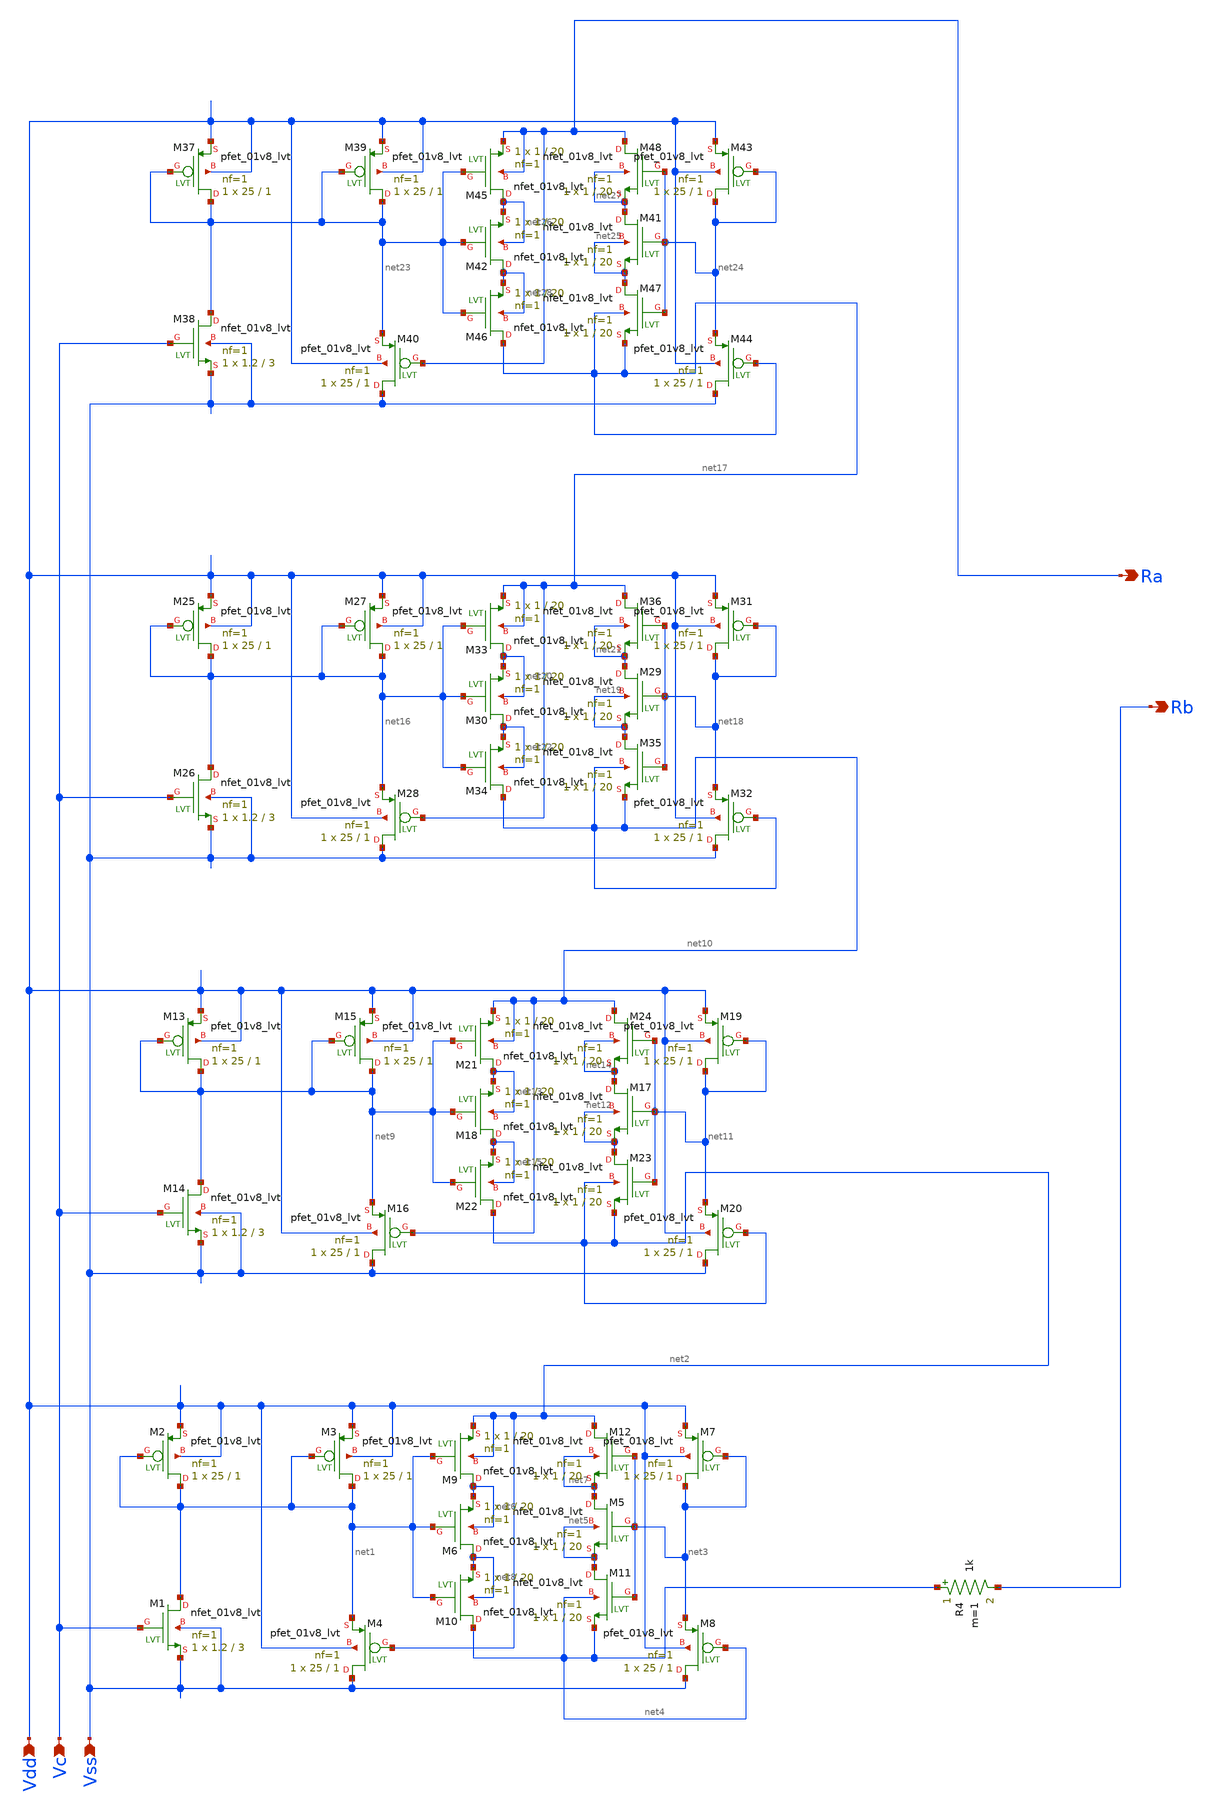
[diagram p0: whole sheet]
** sch_path: xschem/Active_Res.sch
**.subckt Active_Res Vss Vdd Vc Ra Rb
*.ipin Vss
*.ipin Vdd
*.ipin Vc
*.opin Ra
*.opin Rb
XM2 net1 net1 Vdd Vdd sky130_fd_pr__pfet_01v8_lvt L=1 W=25 nf=1 ad='int((1 + 1)/2) * 25 / 1 * 0.29' as='int((1 + 2)/2) * 25 / 1 * 0.29'
+ pd='2*int((1 + 1)/2) * (25 / 1 + 0.29)' ps='2*int((1 + 2)/2) * (25 / 1 + 0.29)' nrd='0.29 / 25 ' nrs='0.29 / 25 '
+ sa=0 sb=0 sd=0 mult=1 m=1
XM1 net1 Vc Vss Vss sky130_fd_pr__nfet_01v8_lvt L=3 W=1.2 nf=1 ad='int((1 + 1)/2) * 1.2 / 1 * 0.29' as='int((1 + 2)/2) * 1.2 / 1 * 0.29'
+ pd='2*int((1 + 1)/2) * (1.2 / 1 + 0.29)' ps='2*int((1 + 2)/2) * (1.2 / 1 + 0.29)' nrd='0.29 / 1.2 ' nrs='0.29 / 1.2 '
+ sa=0 sb=0 sd=0 mult=1 m=1
XM3 net1 net1 Vdd Vdd sky130_fd_pr__pfet_01v8_lvt L=1 W=25 nf=1 ad='int((1 + 1)/2) * 25 / 1 * 0.29' as='int((1 + 2)/2) * 25 / 1 * 0.29'
+ pd='2*int((1 + 1)/2) * (25 / 1 + 0.29)' ps='2*int((1 + 2)/2) * (25 / 1 + 0.29)' nrd='0.29 / 25 ' nrs='0.29 / 25 '
+ sa=0 sb=0 sd=0 mult=1 m=1
XM4 Vss net2 net1 Vdd sky130_fd_pr__pfet_01v8_lvt L=1 W=25 nf=1 ad='int((1 + 1)/2) * 25 / 1 * 0.29' as='int((1 + 2)/2) * 25 / 1 * 0.29'
+ pd='2*int((1 + 1)/2) * (25 / 1 + 0.29)' ps='2*int((1 + 2)/2) * (25 / 1 + 0.29)' nrd='0.29 / 25 ' nrs='0.29 / 25 '
+ sa=0 sb=0 sd=0 mult=1 m=1
XM5 net7 net3 net5 net5 sky130_fd_pr__nfet_01v8_lvt L=20 W=1 nf=1 ad='int((1 + 1)/2) * 1 / 1 * 0.29'
+ as='int((1 + 2)/2) * 1 / 1 * 0.29' pd='2*int((1 + 1)/2) * (1 / 1 + 0.29)' ps='2*int((1 + 2)/2) * (1 / 1 + 0.29)'
+ nrd='0.29 / 1 ' nrs='0.29 / 1 ' sa=0 sb=0 sd=0 mult=1 m=1
XM6 net8 net1 net6 net6 sky130_fd_pr__nfet_01v8_lvt L=20 W=1 nf=1 ad='int((1 + 1)/2) * 1 / 1 * 0.29'
+ as='int((1 + 2)/2) * 1 / 1 * 0.29' pd='2*int((1 + 1)/2) * (1 / 1 + 0.29)' ps='2*int((1 + 2)/2) * (1 / 1 + 0.29)'
+ nrd='0.29 / 1 ' nrs='0.29 / 1 ' sa=0 sb=0 sd=0 mult=1 m=1
XM7 net3 net3 Vdd Vdd sky130_fd_pr__pfet_01v8_lvt L=1 W=25 nf=1 ad='int((1 + 1)/2) * 25 / 1 * 0.29' as='int((1 + 2)/2) * 25 / 1 * 0.29'
+ pd='2*int((1 + 1)/2) * (25 / 1 + 0.29)' ps='2*int((1 + 2)/2) * (25 / 1 + 0.29)' nrd='0.29 / 25 ' nrs='0.29 / 25 '
+ sa=0 sb=0 sd=0 mult=1 m=1
XM8 Vss net4 net3 Vdd sky130_fd_pr__pfet_01v8_lvt L=1 W=25 nf=1 ad='int((1 + 1)/2) * 25 / 1 * 0.29' as='int((1 + 2)/2) * 25 / 1 * 0.29'
+ pd='2*int((1 + 1)/2) * (25 / 1 + 0.29)' ps='2*int((1 + 2)/2) * (25 / 1 + 0.29)' nrd='0.29 / 25 ' nrs='0.29 / 25 '
+ sa=0 sb=0 sd=0 mult=1 m=1
R4 net4 Rb 1k m=1
XM9 net6 net1 net2 net2 sky130_fd_pr__nfet_01v8_lvt L=20 W=1 nf=1 ad='int((1 + 1)/2) * 1 / 1 * 0.29'
+ as='int((1 + 2)/2) * 1 / 1 * 0.29' pd='2*int((1 + 1)/2) * (1 / 1 + 0.29)' ps='2*int((1 + 2)/2) * (1 / 1 + 0.29)'
+ nrd='0.29 / 1 ' nrs='0.29 / 1 ' sa=0 sb=0 sd=0 mult=1 m=1
XM10 net4 net1 net8 net8 sky130_fd_pr__nfet_01v8_lvt L=20 W=1 nf=1 ad='int((1 + 1)/2) * 1 / 1 * 0.29'
+ as='int((1 + 2)/2) * 1 / 1 * 0.29' pd='2*int((1 + 1)/2) * (1 / 1 + 0.29)' ps='2*int((1 + 2)/2) * (1 / 1 + 0.29)'
+ nrd='0.29 / 1 ' nrs='0.29 / 1 ' sa=0 sb=0 sd=0 mult=1 m=1
XM11 net5 net3 net4 net4 sky130_fd_pr__nfet_01v8_lvt L=20 W=1 nf=1 ad='int((1 + 1)/2) * 1 / 1 * 0.29'
+ as='int((1 + 2)/2) * 1 / 1 * 0.29' pd='2*int((1 + 1)/2) * (1 / 1 + 0.29)' ps='2*int((1 + 2)/2) * (1 / 1 + 0.29)'
+ nrd='0.29 / 1 ' nrs='0.29 / 1 ' sa=0 sb=0 sd=0 mult=1 m=1
XM12 net2 net3 net7 net7 sky130_fd_pr__nfet_01v8_lvt L=20 W=1 nf=1 ad='int((1 + 1)/2) * 1 / 1 * 0.29'
+ as='int((1 + 2)/2) * 1 / 1 * 0.29' pd='2*int((1 + 1)/2) * (1 / 1 + 0.29)' ps='2*int((1 + 2)/2) * (1 / 1 + 0.29)'
+ nrd='0.29 / 1 ' nrs='0.29 / 1 ' sa=0 sb=0 sd=0 mult=1 m=1
XM13 net9 net9 Vdd Vdd sky130_fd_pr__pfet_01v8_lvt L=1 W=25 nf=1 ad='int((1 + 1)/2) * 25 / 1 * 0.29'
+ as='int((1 + 2)/2) * 25 / 1 * 0.29' pd='2*int((1 + 1)/2) * (25 / 1 + 0.29)' ps='2*int((1 + 2)/2) * (25 / 1 + 0.29)'
+ nrd='0.29 / 25 ' nrs='0.29 / 25 ' sa=0 sb=0 sd=0 mult=1 m=1
XM14 net9 Vc Vss Vss sky130_fd_pr__nfet_01v8_lvt L=3 W=1.2 nf=1 ad='int((1 + 1)/2) * 1.2 / 1 * 0.29'
+ as='int((1 + 2)/2) * 1.2 / 1 * 0.29' pd='2*int((1 + 1)/2) * (1.2 / 1 + 0.29)' ps='2*int((1 + 2)/2) * (1.2 / 1 + 0.29)'
+ nrd='0.29 / 1.2 ' nrs='0.29 / 1.2 ' sa=0 sb=0 sd=0 mult=1 m=1
XM15 net9 net9 Vdd Vdd sky130_fd_pr__pfet_01v8_lvt L=1 W=25 nf=1 ad='int((1 + 1)/2) * 25 / 1 * 0.29'
+ as='int((1 + 2)/2) * 25 / 1 * 0.29' pd='2*int((1 + 1)/2) * (25 / 1 + 0.29)' ps='2*int((1 + 2)/2) * (25 / 1 + 0.29)'
+ nrd='0.29 / 25 ' nrs='0.29 / 25 ' sa=0 sb=0 sd=0 mult=1 m=1
XM16 Vss net10 net9 Vdd sky130_fd_pr__pfet_01v8_lvt L=1 W=25 nf=1 ad='int((1 + 1)/2) * 25 / 1 * 0.29'
+ as='int((1 + 2)/2) * 25 / 1 * 0.29' pd='2*int((1 + 1)/2) * (25 / 1 + 0.29)' ps='2*int((1 + 2)/2) * (25 / 1 + 0.29)'
+ nrd='0.29 / 25 ' nrs='0.29 / 25 ' sa=0 sb=0 sd=0 mult=1 m=1
XM17 net14 net11 net12 net12 sky130_fd_pr__nfet_01v8_lvt L=20 W=1 nf=1 ad='int((1 + 1)/2) * 1 / 1 * 0.29'
+ as='int((1 + 2)/2) * 1 / 1 * 0.29' pd='2*int((1 + 1)/2) * (1 / 1 + 0.29)' ps='2*int((1 + 2)/2) * (1 / 1 + 0.29)'
+ nrd='0.29 / 1 ' nrs='0.29 / 1 ' sa=0 sb=0 sd=0 mult=1 m=1
XM18 net15 net9 net13 net13 sky130_fd_pr__nfet_01v8_lvt L=20 W=1 nf=1 ad='int((1 + 1)/2) * 1 / 1 * 0.29'
+ as='int((1 + 2)/2) * 1 / 1 * 0.29' pd='2*int((1 + 1)/2) * (1 / 1 + 0.29)' ps='2*int((1 + 2)/2) * (1 / 1 + 0.29)'
+ nrd='0.29 / 1 ' nrs='0.29 / 1 ' sa=0 sb=0 sd=0 mult=1 m=1
XM19 net11 net11 Vdd Vdd sky130_fd_pr__pfet_01v8_lvt L=1 W=25 nf=1 ad='int((1 + 1)/2) * 25 / 1 * 0.29'
+ as='int((1 + 2)/2) * 25 / 1 * 0.29' pd='2*int((1 + 1)/2) * (25 / 1 + 0.29)' ps='2*int((1 + 2)/2) * (25 / 1 + 0.29)'
+ nrd='0.29 / 25 ' nrs='0.29 / 25 ' sa=0 sb=0 sd=0 mult=1 m=1
XM20 Vss net2 net11 Vdd sky130_fd_pr__pfet_01v8_lvt L=1 W=25 nf=1 ad='int((1 + 1)/2) * 25 / 1 * 0.29'
+ as='int((1 + 2)/2) * 25 / 1 * 0.29' pd='2*int((1 + 1)/2) * (25 / 1 + 0.29)' ps='2*int((1 + 2)/2) * (25 / 1 + 0.29)'
+ nrd='0.29 / 25 ' nrs='0.29 / 25 ' sa=0 sb=0 sd=0 mult=1 m=1
XM21 net13 net9 net10 net10 sky130_fd_pr__nfet_01v8_lvt L=20 W=1 nf=1 ad='int((1 + 1)/2) * 1 / 1 * 0.29'
+ as='int((1 + 2)/2) * 1 / 1 * 0.29' pd='2*int((1 + 1)/2) * (1 / 1 + 0.29)' ps='2*int((1 + 2)/2) * (1 / 1 + 0.29)'
+ nrd='0.29 / 1 ' nrs='0.29 / 1 ' sa=0 sb=0 sd=0 mult=1 m=1
XM22 net2 net9 net15 net15 sky130_fd_pr__nfet_01v8_lvt L=20 W=1 nf=1 ad='int((1 + 1)/2) * 1 / 1 * 0.29'
+ as='int((1 + 2)/2) * 1 / 1 * 0.29' pd='2*int((1 + 1)/2) * (1 / 1 + 0.29)' ps='2*int((1 + 2)/2) * (1 / 1 + 0.29)'
+ nrd='0.29 / 1 ' nrs='0.29 / 1 ' sa=0 sb=0 sd=0 mult=1 m=1
XM23 net12 net11 net2 net2 sky130_fd_pr__nfet_01v8_lvt L=20 W=1 nf=1 ad='int((1 + 1)/2) * 1 / 1 * 0.29'
+ as='int((1 + 2)/2) * 1 / 1 * 0.29' pd='2*int((1 + 1)/2) * (1 / 1 + 0.29)' ps='2*int((1 + 2)/2) * (1 / 1 + 0.29)'
+ nrd='0.29 / 1 ' nrs='0.29 / 1 ' sa=0 sb=0 sd=0 mult=1 m=1
XM24 net10 net11 net14 net14 sky130_fd_pr__nfet_01v8_lvt L=20 W=1 nf=1 ad='int((1 + 1)/2) * 1 / 1 * 0.29'
+ as='int((1 + 2)/2) * 1 / 1 * 0.29' pd='2*int((1 + 1)/2) * (1 / 1 + 0.29)' ps='2*int((1 + 2)/2) * (1 / 1 + 0.29)'
+ nrd='0.29 / 1 ' nrs='0.29 / 1 ' sa=0 sb=0 sd=0 mult=1 m=1
XM25 net16 net16 Vdd Vdd sky130_fd_pr__pfet_01v8_lvt L=1 W=25 nf=1 ad='int((1 + 1)/2) * 25 / 1 * 0.29'
+ as='int((1 + 2)/2) * 25 / 1 * 0.29' pd='2*int((1 + 1)/2) * (25 / 1 + 0.29)' ps='2*int((1 + 2)/2) * (25 / 1 + 0.29)'
+ nrd='0.29 / 25 ' nrs='0.29 / 25 ' sa=0 sb=0 sd=0 mult=1 m=1
XM26 net16 Vc Vss Vss sky130_fd_pr__nfet_01v8_lvt L=3 W=1.2 nf=1 ad='int((1 + 1)/2) * 1.2 / 1 * 0.29'
+ as='int((1 + 2)/2) * 1.2 / 1 * 0.29' pd='2*int((1 + 1)/2) * (1.2 / 1 + 0.29)' ps='2*int((1 + 2)/2) * (1.2 / 1 + 0.29)'
+ nrd='0.29 / 1.2 ' nrs='0.29 / 1.2 ' sa=0 sb=0 sd=0 mult=1 m=1
XM27 net16 net16 Vdd Vdd sky130_fd_pr__pfet_01v8_lvt L=1 W=25 nf=1 ad='int((1 + 1)/2) * 25 / 1 * 0.29'
+ as='int((1 + 2)/2) * 25 / 1 * 0.29' pd='2*int((1 + 1)/2) * (25 / 1 + 0.29)' ps='2*int((1 + 2)/2) * (25 / 1 + 0.29)'
+ nrd='0.29 / 25 ' nrs='0.29 / 25 ' sa=0 sb=0 sd=0 mult=1 m=1
XM28 Vss net17 net16 Vdd sky130_fd_pr__pfet_01v8_lvt L=1 W=25 nf=1 ad='int((1 + 1)/2) * 25 / 1 * 0.29'
+ as='int((1 + 2)/2) * 25 / 1 * 0.29' pd='2*int((1 + 1)/2) * (25 / 1 + 0.29)' ps='2*int((1 + 2)/2) * (25 / 1 + 0.29)'
+ nrd='0.29 / 25 ' nrs='0.29 / 25 ' sa=0 sb=0 sd=0 mult=1 m=1
XM29 net21 net18 net19 net19 sky130_fd_pr__nfet_01v8_lvt L=20 W=1 nf=1 ad='int((1 + 1)/2) * 1 / 1 * 0.29'
+ as='int((1 + 2)/2) * 1 / 1 * 0.29' pd='2*int((1 + 1)/2) * (1 / 1 + 0.29)' ps='2*int((1 + 2)/2) * (1 / 1 + 0.29)'
+ nrd='0.29 / 1 ' nrs='0.29 / 1 ' sa=0 sb=0 sd=0 mult=1 m=1
XM30 net22 net16 net20 net20 sky130_fd_pr__nfet_01v8_lvt L=20 W=1 nf=1 ad='int((1 + 1)/2) * 1 / 1 * 0.29'
+ as='int((1 + 2)/2) * 1 / 1 * 0.29' pd='2*int((1 + 1)/2) * (1 / 1 + 0.29)' ps='2*int((1 + 2)/2) * (1 / 1 + 0.29)'
+ nrd='0.29 / 1 ' nrs='0.29 / 1 ' sa=0 sb=0 sd=0 mult=1 m=1
XM31 net18 net18 Vdd Vdd sky130_fd_pr__pfet_01v8_lvt L=1 W=25 nf=1 ad='int((1 + 1)/2) * 25 / 1 * 0.29'
+ as='int((1 + 2)/2) * 25 / 1 * 0.29' pd='2*int((1 + 1)/2) * (25 / 1 + 0.29)' ps='2*int((1 + 2)/2) * (25 / 1 + 0.29)'
+ nrd='0.29 / 25 ' nrs='0.29 / 25 ' sa=0 sb=0 sd=0 mult=1 m=1
XM32 Vss net10 net18 Vdd sky130_fd_pr__pfet_01v8_lvt L=1 W=25 nf=1 ad='int((1 + 1)/2) * 25 / 1 * 0.29'
+ as='int((1 + 2)/2) * 25 / 1 * 0.29' pd='2*int((1 + 1)/2) * (25 / 1 + 0.29)' ps='2*int((1 + 2)/2) * (25 / 1 + 0.29)'
+ nrd='0.29 / 25 ' nrs='0.29 / 25 ' sa=0 sb=0 sd=0 mult=1 m=1
XM33 net20 net16 net17 net17 sky130_fd_pr__nfet_01v8_lvt L=20 W=1 nf=1 ad='int((1 + 1)/2) * 1 / 1 * 0.29'
+ as='int((1 + 2)/2) * 1 / 1 * 0.29' pd='2*int((1 + 1)/2) * (1 / 1 + 0.29)' ps='2*int((1 + 2)/2) * (1 / 1 + 0.29)'
+ nrd='0.29 / 1 ' nrs='0.29 / 1 ' sa=0 sb=0 sd=0 mult=1 m=1
XM34 net10 net16 net22 net22 sky130_fd_pr__nfet_01v8_lvt L=20 W=1 nf=1 ad='int((1 + 1)/2) * 1 / 1 * 0.29'
+ as='int((1 + 2)/2) * 1 / 1 * 0.29' pd='2*int((1 + 1)/2) * (1 / 1 + 0.29)' ps='2*int((1 + 2)/2) * (1 / 1 + 0.29)'
+ nrd='0.29 / 1 ' nrs='0.29 / 1 ' sa=0 sb=0 sd=0 mult=1 m=1
XM35 net19 net18 net10 net10 sky130_fd_pr__nfet_01v8_lvt L=20 W=1 nf=1 ad='int((1 + 1)/2) * 1 / 1 * 0.29'
+ as='int((1 + 2)/2) * 1 / 1 * 0.29' pd='2*int((1 + 1)/2) * (1 / 1 + 0.29)' ps='2*int((1 + 2)/2) * (1 / 1 + 0.29)'
+ nrd='0.29 / 1 ' nrs='0.29 / 1 ' sa=0 sb=0 sd=0 mult=1 m=1
XM36 net17 net18 net21 net21 sky130_fd_pr__nfet_01v8_lvt L=20 W=1 nf=1 ad='int((1 + 1)/2) * 1 / 1 * 0.29'
+ as='int((1 + 2)/2) * 1 / 1 * 0.29' pd='2*int((1 + 1)/2) * (1 / 1 + 0.29)' ps='2*int((1 + 2)/2) * (1 / 1 + 0.29)'
+ nrd='0.29 / 1 ' nrs='0.29 / 1 ' sa=0 sb=0 sd=0 mult=1 m=1
XM37 net23 net23 Vdd Vdd sky130_fd_pr__pfet_01v8_lvt L=1 W=25 nf=1 ad='int((1 + 1)/2) * 25 / 1 * 0.29'
+ as='int((1 + 2)/2) * 25 / 1 * 0.29' pd='2*int((1 + 1)/2) * (25 / 1 + 0.29)' ps='2*int((1 + 2)/2) * (25 / 1 + 0.29)'
+ nrd='0.29 / 25 ' nrs='0.29 / 25 ' sa=0 sb=0 sd=0 mult=1 m=1
XM38 net23 Vc Vss Vss sky130_fd_pr__nfet_01v8_lvt L=3 W=1.2 nf=1 ad='int((1 + 1)/2) * 1.2 / 1 * 0.29'
+ as='int((1 + 2)/2) * 1.2 / 1 * 0.29' pd='2*int((1 + 1)/2) * (1.2 / 1 + 0.29)' ps='2*int((1 + 2)/2) * (1.2 / 1 + 0.29)'
+ nrd='0.29 / 1.2 ' nrs='0.29 / 1.2 ' sa=0 sb=0 sd=0 mult=1 m=1
XM39 net23 net23 Vdd Vdd sky130_fd_pr__pfet_01v8_lvt L=1 W=25 nf=1 ad='int((1 + 1)/2) * 25 / 1 * 0.29'
+ as='int((1 + 2)/2) * 25 / 1 * 0.29' pd='2*int((1 + 1)/2) * (25 / 1 + 0.29)' ps='2*int((1 + 2)/2) * (25 / 1 + 0.29)'
+ nrd='0.29 / 25 ' nrs='0.29 / 25 ' sa=0 sb=0 sd=0 mult=1 m=1
XM40 Vss Ra net23 Vdd sky130_fd_pr__pfet_01v8_lvt L=1 W=25 nf=1 ad='int((1 + 1)/2) * 25 / 1 * 0.29' as='int((1 + 2)/2) * 25 / 1 * 0.29'
+ pd='2*int((1 + 1)/2) * (25 / 1 + 0.29)' ps='2*int((1 + 2)/2) * (25 / 1 + 0.29)' nrd='0.29 / 25 ' nrs='0.29 / 25 '
+ sa=0 sb=0 sd=0 mult=1 m=1
XM41 net27 net24 net25 net25 sky130_fd_pr__nfet_01v8_lvt L=20 W=1 nf=1 ad='int((1 + 1)/2) * 1 / 1 * 0.29'
+ as='int((1 + 2)/2) * 1 / 1 * 0.29' pd='2*int((1 + 1)/2) * (1 / 1 + 0.29)' ps='2*int((1 + 2)/2) * (1 / 1 + 0.29)'
+ nrd='0.29 / 1 ' nrs='0.29 / 1 ' sa=0 sb=0 sd=0 mult=1 m=1
XM42 net28 net23 net26 net26 sky130_fd_pr__nfet_01v8_lvt L=20 W=1 nf=1 ad='int((1 + 1)/2) * 1 / 1 * 0.29'
+ as='int((1 + 2)/2) * 1 / 1 * 0.29' pd='2*int((1 + 1)/2) * (1 / 1 + 0.29)' ps='2*int((1 + 2)/2) * (1 / 1 + 0.29)'
+ nrd='0.29 / 1 ' nrs='0.29 / 1 ' sa=0 sb=0 sd=0 mult=1 m=1
XM43 net24 net24 Vdd Vdd sky130_fd_pr__pfet_01v8_lvt L=1 W=25 nf=1 ad='int((1 + 1)/2) * 25 / 1 * 0.29'
+ as='int((1 + 2)/2) * 25 / 1 * 0.29' pd='2*int((1 + 1)/2) * (25 / 1 + 0.29)' ps='2*int((1 + 2)/2) * (25 / 1 + 0.29)'
+ nrd='0.29 / 25 ' nrs='0.29 / 25 ' sa=0 sb=0 sd=0 mult=1 m=1
XM44 Vss net17 net24 Vdd sky130_fd_pr__pfet_01v8_lvt L=1 W=25 nf=1 ad='int((1 + 1)/2) * 25 / 1 * 0.29'
+ as='int((1 + 2)/2) * 25 / 1 * 0.29' pd='2*int((1 + 1)/2) * (25 / 1 + 0.29)' ps='2*int((1 + 2)/2) * (25 / 1 + 0.29)'
+ nrd='0.29 / 25 ' nrs='0.29 / 25 ' sa=0 sb=0 sd=0 mult=1 m=1
XM45 net26 net23 Ra Ra sky130_fd_pr__nfet_01v8_lvt L=20 W=1 nf=1 ad='int((1 + 1)/2) * 1 / 1 * 0.29' as='int((1 + 2)/2) * 1 / 1 * 0.29'
+ pd='2*int((1 + 1)/2) * (1 / 1 + 0.29)' ps='2*int((1 + 2)/2) * (1 / 1 + 0.29)' nrd='0.29 / 1 ' nrs='0.29 / 1 '
+ sa=0 sb=0 sd=0 mult=1 m=1
XM46 net17 net23 net28 net28 sky130_fd_pr__nfet_01v8_lvt L=20 W=1 nf=1 ad='int((1 + 1)/2) * 1 / 1 * 0.29'
+ as='int((1 + 2)/2) * 1 / 1 * 0.29' pd='2*int((1 + 1)/2) * (1 / 1 + 0.29)' ps='2*int((1 + 2)/2) * (1 / 1 + 0.29)'
+ nrd='0.29 / 1 ' nrs='0.29 / 1 ' sa=0 sb=0 sd=0 mult=1 m=1
XM47 net25 net24 net17 net17 sky130_fd_pr__nfet_01v8_lvt L=20 W=1 nf=1 ad='int((1 + 1)/2) * 1 / 1 * 0.29'
+ as='int((1 + 2)/2) * 1 / 1 * 0.29' pd='2*int((1 + 1)/2) * (1 / 1 + 0.29)' ps='2*int((1 + 2)/2) * (1 / 1 + 0.29)'
+ nrd='0.29 / 1 ' nrs='0.29 / 1 ' sa=0 sb=0 sd=0 mult=1 m=1
XM48 Ra net24 net27 net27 sky130_fd_pr__nfet_01v8_lvt L=20 W=1 nf=1 ad='int((1 + 1)/2) * 1 / 1 * 0.29'
+ as='int((1 + 2)/2) * 1 / 1 * 0.29' pd='2*int((1 + 1)/2) * (1 / 1 + 0.29)' ps='2*int((1 + 2)/2) * (1 / 1 + 0.29)'
+ nrd='0.29 / 1 ' nrs='0.29 / 1 ' sa=0 sb=0 sd=0 mult=1 m=1
**.ends
.end
